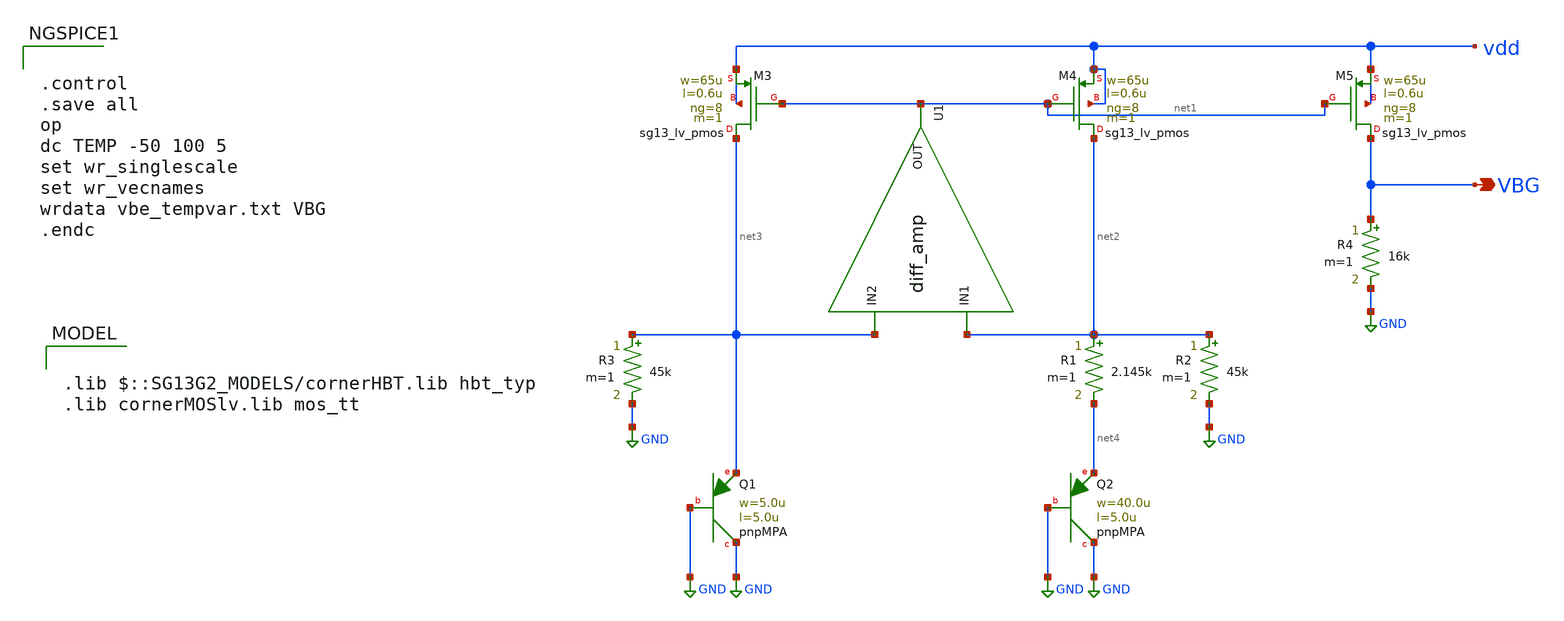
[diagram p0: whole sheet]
** sch_path: modules/module_1_bandgap_reference/part_2_full_bgr/schematic/bandgap_ref.sch
**.subckt bandgap_ref VBG
*.opin VBG
XM3 net3 net1 vdd vdd sg13_lv_pmos w=65u l=0.6u ng=8 m=1 mm_ok=1
XM4 net2 net1 vdd vdd sg13_lv_pmos w=65u l=0.6u ng=8 m=1 mm_ok=1
XU1 net1 net2 net3 diff_amp_cell
XM5 VBG net1 vdd vdd sg13_lv_pmos w=65u l=0.6u ng=8 m=1 mm_ok=1
R4 VBG GND 16k m=1
R3 net3 GND 45k m=1
R1 net2 net4 2.145k m=1
R2 net2 GND 45k m=1
XQ1 GND GND net3 pnpMPA a=25p p=20u m=1
XQ2 GND GND net4 pnpMPA a=200p p=90u m=1
**** begin user architecture code

.lib $::SG13G2_MODELS/cornerHBT.lib hbt_typ
.lib cornerMOSlv.lib mos_tt



.control
.save all
op
dc TEMP -50 100 5
set wr_singlescale
set wr_vecnames
wrdata vbe_tempvar.txt VBG
.endc



**** end user architecture code
**.ends
.GLOBAL GND
**** begin user architecture code


.subckt diff_amp_cell OUT IN1 IN2

N1 out in1 in2 diff_amp_model

.ends diff_amp_cell



.model diff_amp_model diff_amp



.control

* following line specifies the location for the .osdi file so ngspice can use it.

pre_osdi
+ /home/pedersen/chipdesign/cmos_analog/opensource_analog_course/bgr_bjt/verilog/diff_amp.osdi

.endc


**** end user architecture code
.end
